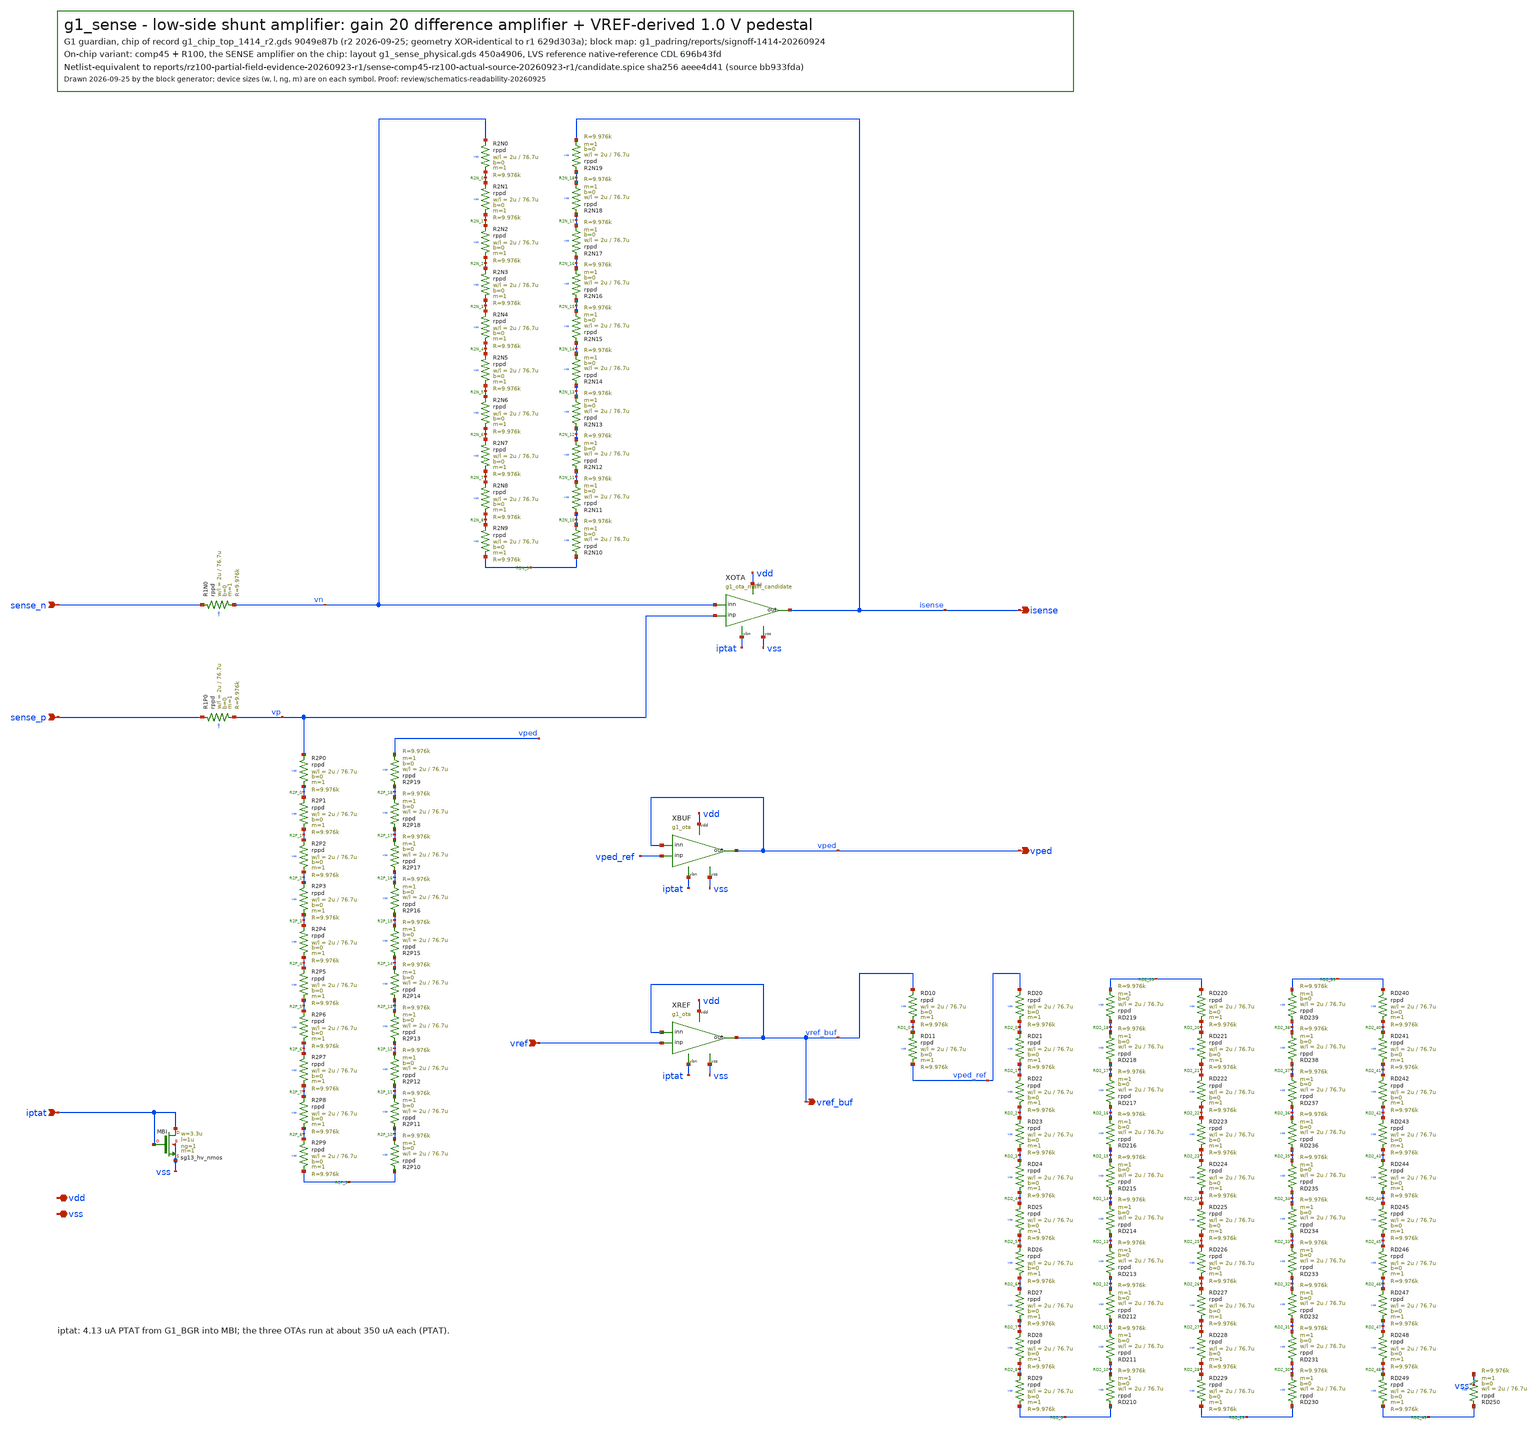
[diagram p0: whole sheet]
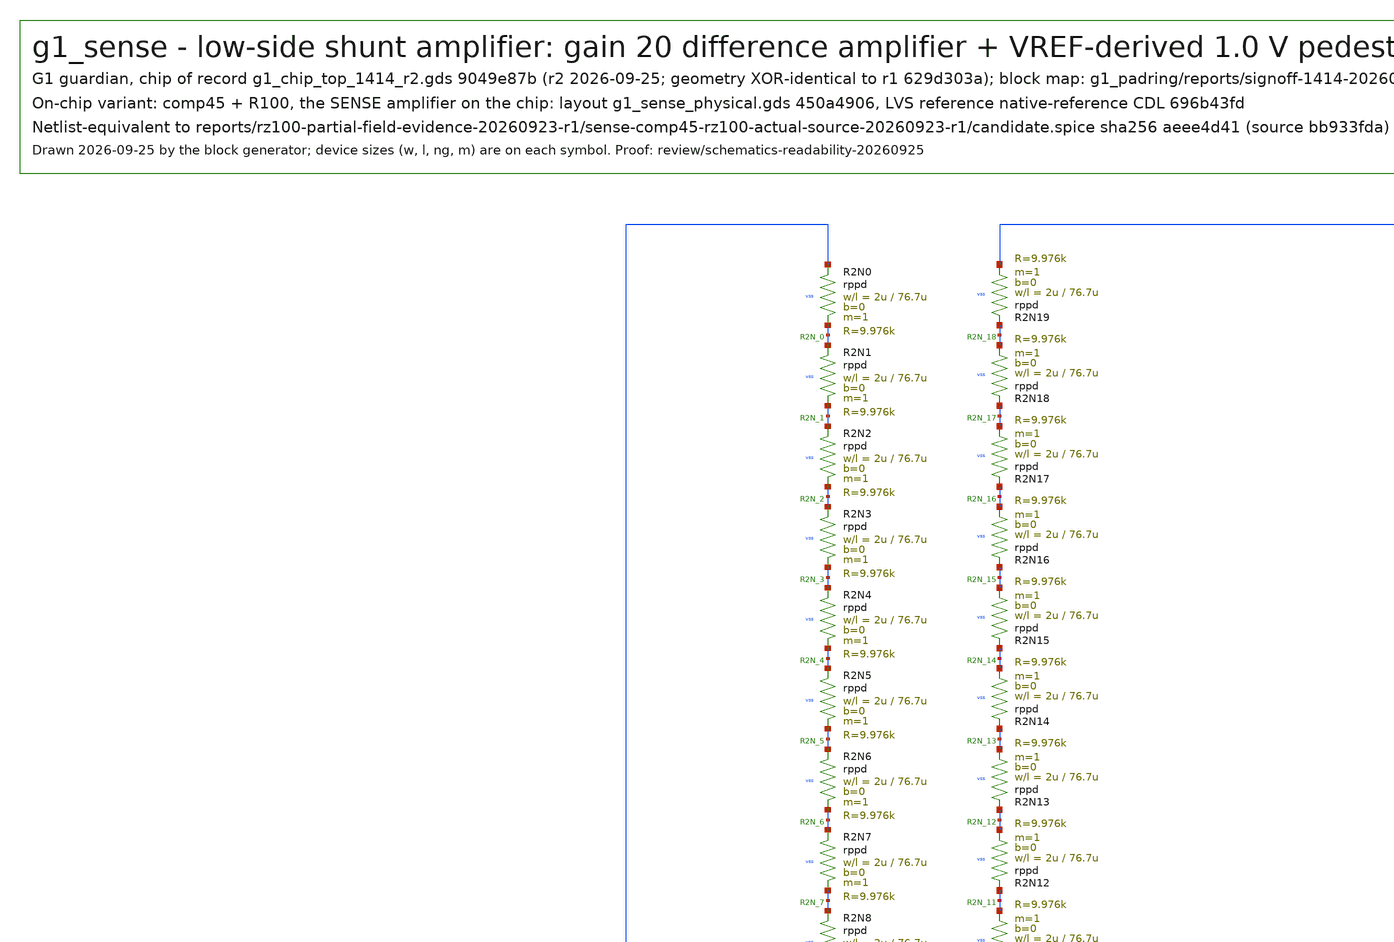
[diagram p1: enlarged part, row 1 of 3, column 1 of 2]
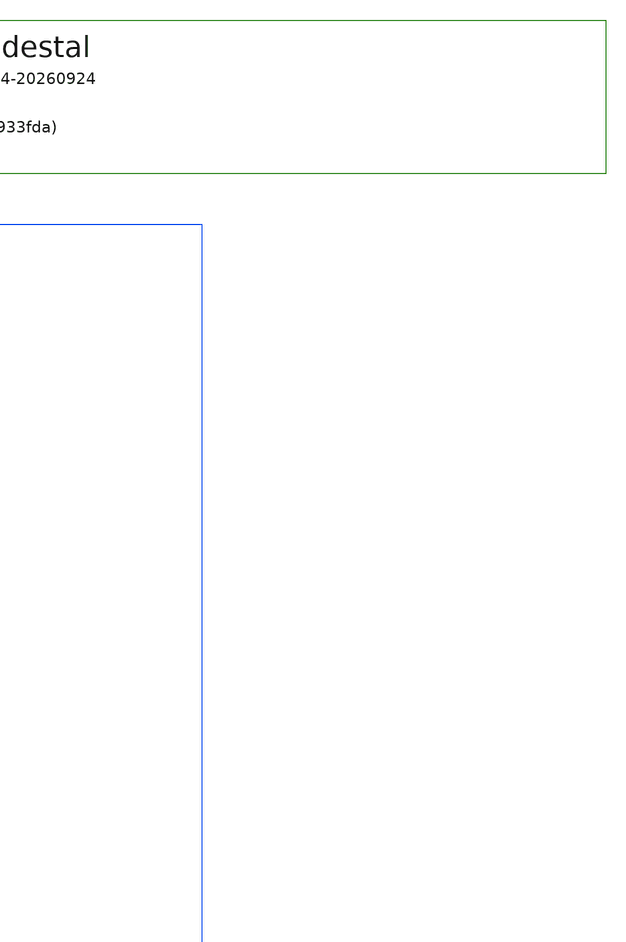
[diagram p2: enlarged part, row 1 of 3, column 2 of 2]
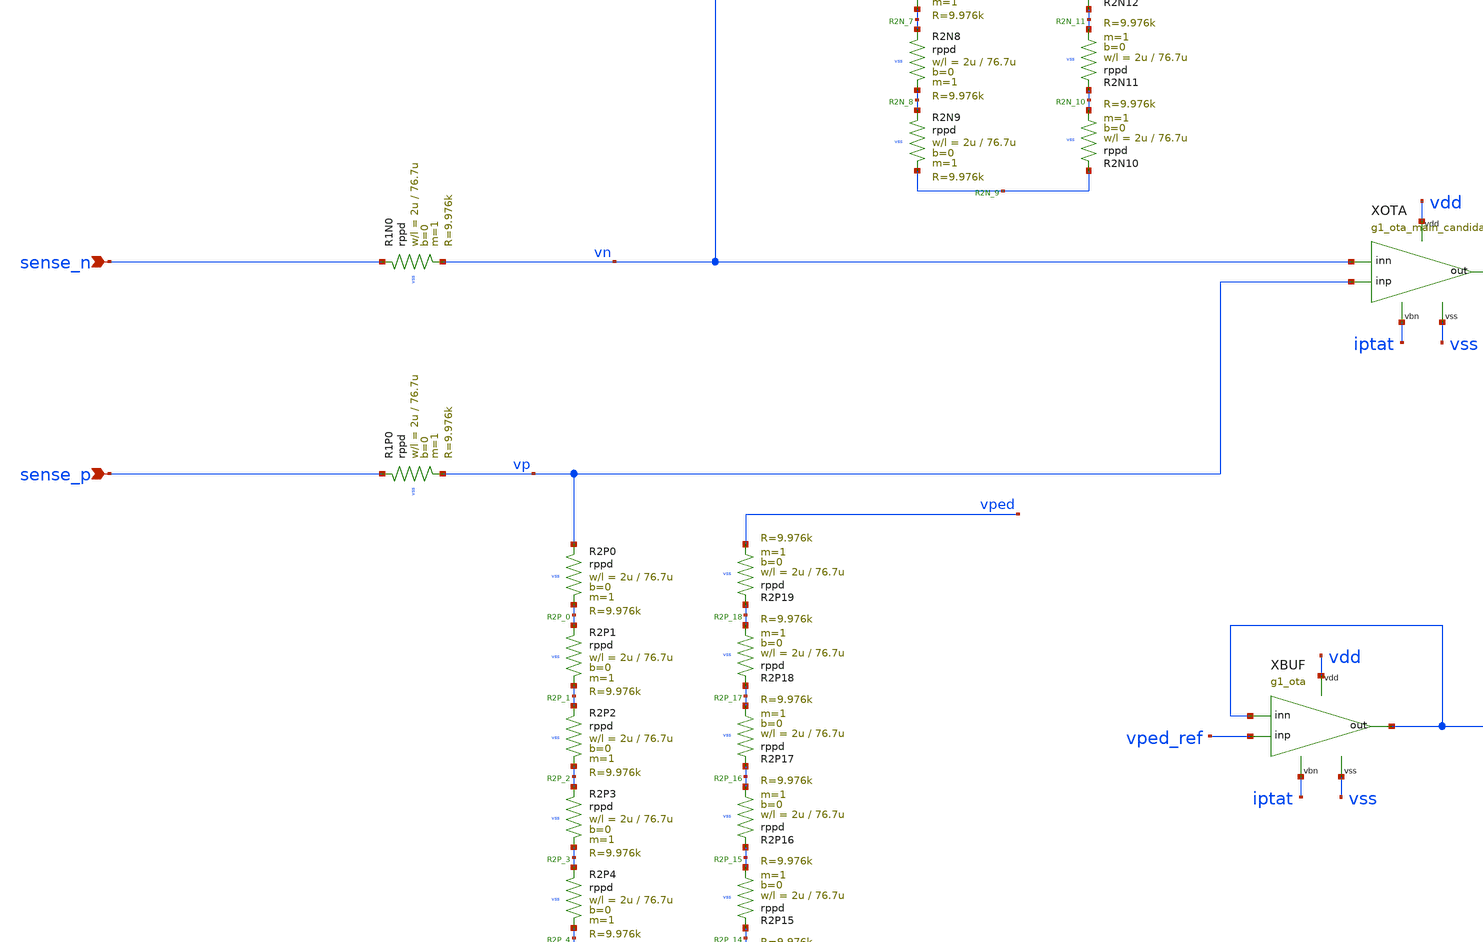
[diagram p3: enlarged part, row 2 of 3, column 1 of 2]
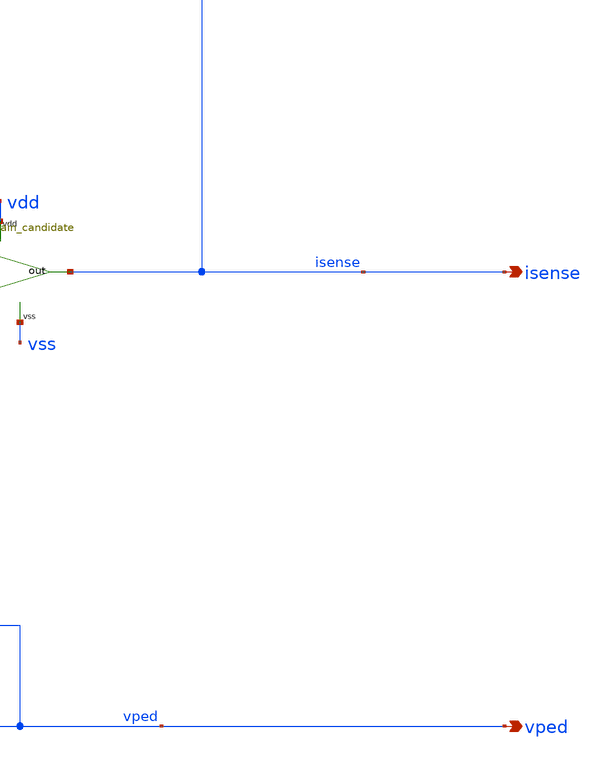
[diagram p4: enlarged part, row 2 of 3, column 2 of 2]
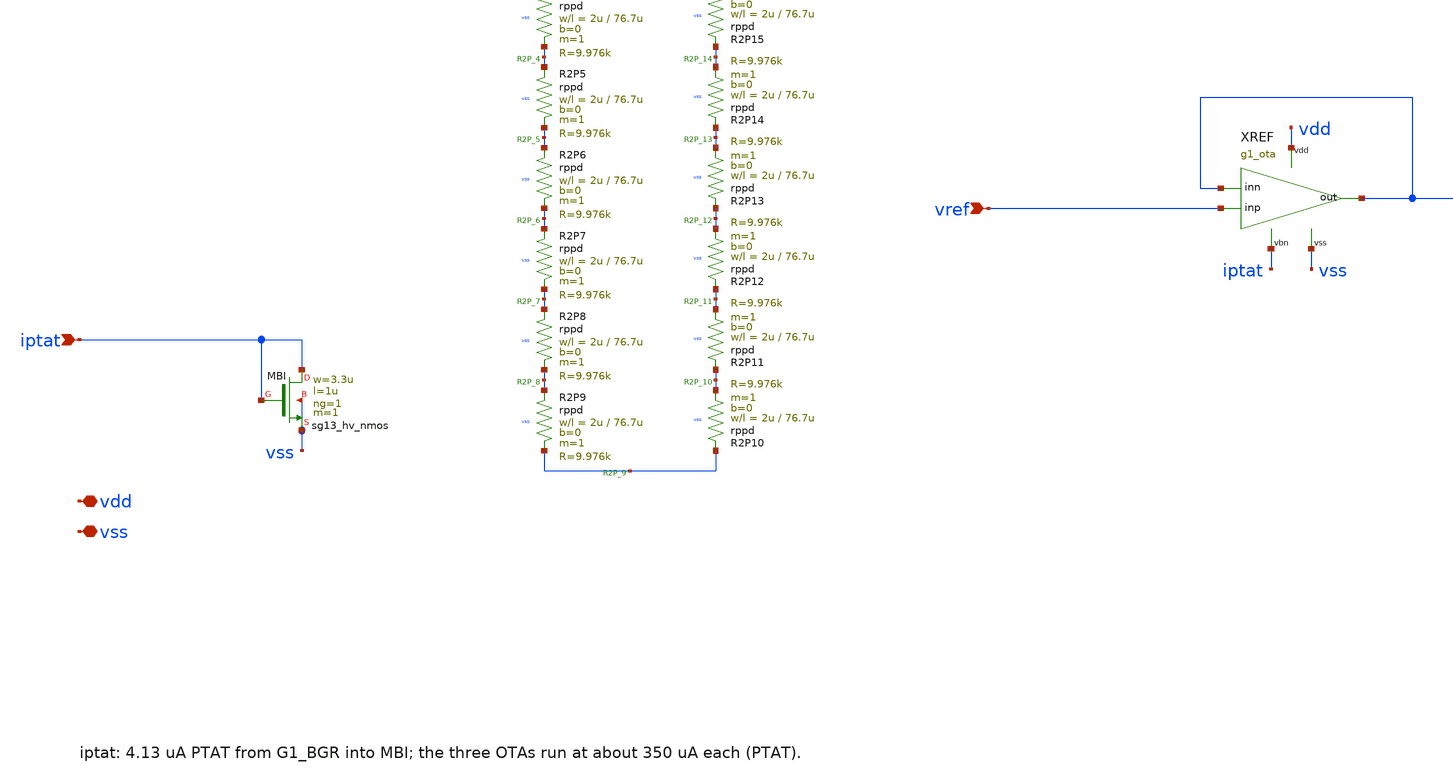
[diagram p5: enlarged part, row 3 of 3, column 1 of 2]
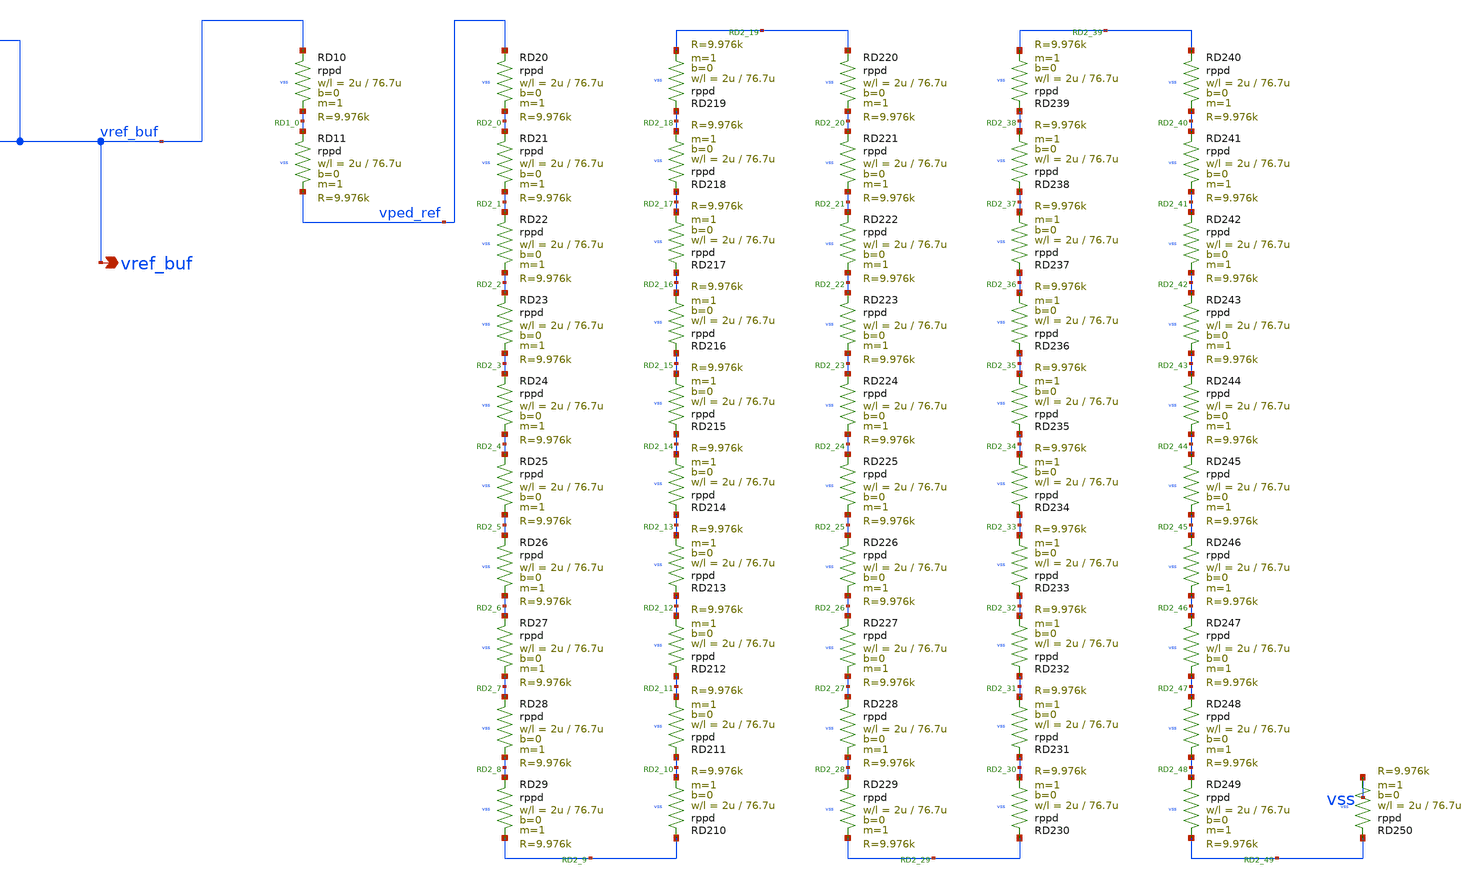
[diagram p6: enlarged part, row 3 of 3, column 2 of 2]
** sch_path: designs/g1-guardian/blocks/g1_sense/xschem/comp45_r100/g1_sense.sch
**.subckt g1_sense sense_p sense_n vref iptat isense vped vref_buf vdd vss
*.ipin sense_p
*.ipin sense_n
*.ipin vref
*.ipin iptat
*.opin isense
*.opin vped
*.opin vref_buf
*.iopin vdd
*.iopin vss
XR1N0 sense_n vn vss rppd w=2u l=76.7u m=1 b=0 mm_ok=1
XR2N0 vn R2N_0 vss rppd w=2u l=76.7u m=1 b=0 mm_ok=1
XR2N1 R2N_0 R2N_1 vss rppd w=2u l=76.7u m=1 b=0 mm_ok=1
XR2N2 R2N_1 R2N_2 vss rppd w=2u l=76.7u m=1 b=0 mm_ok=1
XR2N3 R2N_2 R2N_3 vss rppd w=2u l=76.7u m=1 b=0 mm_ok=1
XR2N4 R2N_3 R2N_4 vss rppd w=2u l=76.7u m=1 b=0 mm_ok=1
XR2N5 R2N_4 R2N_5 vss rppd w=2u l=76.7u m=1 b=0 mm_ok=1
XR2N6 R2N_5 R2N_6 vss rppd w=2u l=76.7u m=1 b=0 mm_ok=1
XR2N7 R2N_6 R2N_7 vss rppd w=2u l=76.7u m=1 b=0 mm_ok=1
XR2N8 R2N_7 R2N_8 vss rppd w=2u l=76.7u m=1 b=0 mm_ok=1
XR2N9 R2N_8 R2N_9 vss rppd w=2u l=76.7u m=1 b=0 mm_ok=1
XR2N10 R2N_9 R2N_10 vss rppd w=2u l=76.7u m=1 b=0 mm_ok=1
XR2N11 R2N_10 R2N_11 vss rppd w=2u l=76.7u m=1 b=0 mm_ok=1
XR2N12 R2N_11 R2N_12 vss rppd w=2u l=76.7u m=1 b=0 mm_ok=1
XR2N13 R2N_12 R2N_13 vss rppd w=2u l=76.7u m=1 b=0 mm_ok=1
XR2N14 R2N_13 R2N_14 vss rppd w=2u l=76.7u m=1 b=0 mm_ok=1
XR2N15 R2N_14 R2N_15 vss rppd w=2u l=76.7u m=1 b=0 mm_ok=1
XR2N16 R2N_15 R2N_16 vss rppd w=2u l=76.7u m=1 b=0 mm_ok=1
XR2N17 R2N_16 R2N_17 vss rppd w=2u l=76.7u m=1 b=0 mm_ok=1
XR2N18 R2N_17 R2N_18 vss rppd w=2u l=76.7u m=1 b=0 mm_ok=1
XR2N19 R2N_18 isense vss rppd w=2u l=76.7u m=1 b=0 mm_ok=1
XR1P0 sense_p vp vss rppd w=2u l=76.7u m=1 b=0 mm_ok=1
XR2P0 vp R2P_0 vss rppd w=2u l=76.7u m=1 b=0 mm_ok=1
XR2P1 R2P_0 R2P_1 vss rppd w=2u l=76.7u m=1 b=0 mm_ok=1
XR2P2 R2P_1 R2P_2 vss rppd w=2u l=76.7u m=1 b=0 mm_ok=1
XR2P3 R2P_2 R2P_3 vss rppd w=2u l=76.7u m=1 b=0 mm_ok=1
XR2P4 R2P_3 R2P_4 vss rppd w=2u l=76.7u m=1 b=0 mm_ok=1
XR2P5 R2P_4 R2P_5 vss rppd w=2u l=76.7u m=1 b=0 mm_ok=1
XR2P6 R2P_5 R2P_6 vss rppd w=2u l=76.7u m=1 b=0 mm_ok=1
XR2P7 R2P_6 R2P_7 vss rppd w=2u l=76.7u m=1 b=0 mm_ok=1
XR2P8 R2P_7 R2P_8 vss rppd w=2u l=76.7u m=1 b=0 mm_ok=1
XR2P9 R2P_8 R2P_9 vss rppd w=2u l=76.7u m=1 b=0 mm_ok=1
XR2P10 R2P_9 R2P_10 vss rppd w=2u l=76.7u m=1 b=0 mm_ok=1
XR2P11 R2P_10 R2P_11 vss rppd w=2u l=76.7u m=1 b=0 mm_ok=1
XR2P12 R2P_11 R2P_12 vss rppd w=2u l=76.7u m=1 b=0 mm_ok=1
XR2P13 R2P_12 R2P_13 vss rppd w=2u l=76.7u m=1 b=0 mm_ok=1
XR2P14 R2P_13 R2P_14 vss rppd w=2u l=76.7u m=1 b=0 mm_ok=1
XR2P15 R2P_14 R2P_15 vss rppd w=2u l=76.7u m=1 b=0 mm_ok=1
XR2P16 R2P_15 R2P_16 vss rppd w=2u l=76.7u m=1 b=0 mm_ok=1
XR2P17 R2P_16 R2P_17 vss rppd w=2u l=76.7u m=1 b=0 mm_ok=1
XR2P18 R2P_17 R2P_18 vss rppd w=2u l=76.7u m=1 b=0 mm_ok=1
XR2P19 R2P_18 vped vss rppd w=2u l=76.7u m=1 b=0 mm_ok=1
XRD10 vref_buf RD1_0 vss rppd w=2u l=76.7u m=1 b=0 mm_ok=1
XRD11 RD1_0 vped_ref vss rppd w=2u l=76.7u m=1 b=0 mm_ok=1
XRD20 vped_ref RD2_0 vss rppd w=2u l=76.7u m=1 b=0 mm_ok=1
XRD21 RD2_0 RD2_1 vss rppd w=2u l=76.7u m=1 b=0 mm_ok=1
XRD22 RD2_1 RD2_2 vss rppd w=2u l=76.7u m=1 b=0 mm_ok=1
XRD23 RD2_2 RD2_3 vss rppd w=2u l=76.7u m=1 b=0 mm_ok=1
XRD24 RD2_3 RD2_4 vss rppd w=2u l=76.7u m=1 b=0 mm_ok=1
XRD25 RD2_4 RD2_5 vss rppd w=2u l=76.7u m=1 b=0 mm_ok=1
XRD26 RD2_5 RD2_6 vss rppd w=2u l=76.7u m=1 b=0 mm_ok=1
XRD27 RD2_6 RD2_7 vss rppd w=2u l=76.7u m=1 b=0 mm_ok=1
XRD28 RD2_7 RD2_8 vss rppd w=2u l=76.7u m=1 b=0 mm_ok=1
XRD29 RD2_8 RD2_9 vss rppd w=2u l=76.7u m=1 b=0 mm_ok=1
XRD210 RD2_9 RD2_10 vss rppd w=2u l=76.7u m=1 b=0 mm_ok=1
XRD211 RD2_10 RD2_11 vss rppd w=2u l=76.7u m=1 b=0 mm_ok=1
XRD212 RD2_11 RD2_12 vss rppd w=2u l=76.7u m=1 b=0 mm_ok=1
XRD213 RD2_12 RD2_13 vss rppd w=2u l=76.7u m=1 b=0 mm_ok=1
XRD214 RD2_13 RD2_14 vss rppd w=2u l=76.7u m=1 b=0 mm_ok=1
XRD215 RD2_14 RD2_15 vss rppd w=2u l=76.7u m=1 b=0 mm_ok=1
XRD216 RD2_15 RD2_16 vss rppd w=2u l=76.7u m=1 b=0 mm_ok=1
XRD217 RD2_16 RD2_17 vss rppd w=2u l=76.7u m=1 b=0 mm_ok=1
XRD218 RD2_17 RD2_18 vss rppd w=2u l=76.7u m=1 b=0 mm_ok=1
XRD219 RD2_18 RD2_19 vss rppd w=2u l=76.7u m=1 b=0 mm_ok=1
XRD220 RD2_19 RD2_20 vss rppd w=2u l=76.7u m=1 b=0 mm_ok=1
XRD221 RD2_20 RD2_21 vss rppd w=2u l=76.7u m=1 b=0 mm_ok=1
XRD222 RD2_21 RD2_22 vss rppd w=2u l=76.7u m=1 b=0 mm_ok=1
XRD223 RD2_22 RD2_23 vss rppd w=2u l=76.7u m=1 b=0 mm_ok=1
XRD224 RD2_23 RD2_24 vss rppd w=2u l=76.7u m=1 b=0 mm_ok=1
XRD225 RD2_24 RD2_25 vss rppd w=2u l=76.7u m=1 b=0 mm_ok=1
XRD226 RD2_25 RD2_26 vss rppd w=2u l=76.7u m=1 b=0 mm_ok=1
XRD227 RD2_26 RD2_27 vss rppd w=2u l=76.7u m=1 b=0 mm_ok=1
XRD228 RD2_27 RD2_28 vss rppd w=2u l=76.7u m=1 b=0 mm_ok=1
XRD229 RD2_28 RD2_29 vss rppd w=2u l=76.7u m=1 b=0 mm_ok=1
XRD230 RD2_29 RD2_30 vss rppd w=2u l=76.7u m=1 b=0 mm_ok=1
XRD231 RD2_30 RD2_31 vss rppd w=2u l=76.7u m=1 b=0 mm_ok=1
XRD232 RD2_31 RD2_32 vss rppd w=2u l=76.7u m=1 b=0 mm_ok=1
XRD233 RD2_32 RD2_33 vss rppd w=2u l=76.7u m=1 b=0 mm_ok=1
XRD234 RD2_33 RD2_34 vss rppd w=2u l=76.7u m=1 b=0 mm_ok=1
XRD235 RD2_34 RD2_35 vss rppd w=2u l=76.7u m=1 b=0 mm_ok=1
XRD236 RD2_35 RD2_36 vss rppd w=2u l=76.7u m=1 b=0 mm_ok=1
XRD237 RD2_36 RD2_37 vss rppd w=2u l=76.7u m=1 b=0 mm_ok=1
XRD238 RD2_37 RD2_38 vss rppd w=2u l=76.7u m=1 b=0 mm_ok=1
XRD239 RD2_38 RD2_39 vss rppd w=2u l=76.7u m=1 b=0 mm_ok=1
XRD240 RD2_39 RD2_40 vss rppd w=2u l=76.7u m=1 b=0 mm_ok=1
XRD241 RD2_40 RD2_41 vss rppd w=2u l=76.7u m=1 b=0 mm_ok=1
XRD242 RD2_41 RD2_42 vss rppd w=2u l=76.7u m=1 b=0 mm_ok=1
XRD243 RD2_42 RD2_43 vss rppd w=2u l=76.7u m=1 b=0 mm_ok=1
XRD244 RD2_43 RD2_44 vss rppd w=2u l=76.7u m=1 b=0 mm_ok=1
XRD245 RD2_44 RD2_45 vss rppd w=2u l=76.7u m=1 b=0 mm_ok=1
XRD246 RD2_45 RD2_46 vss rppd w=2u l=76.7u m=1 b=0 mm_ok=1
XRD247 RD2_46 RD2_47 vss rppd w=2u l=76.7u m=1 b=0 mm_ok=1
XRD248 RD2_47 RD2_48 vss rppd w=2u l=76.7u m=1 b=0 mm_ok=1
XRD249 RD2_48 RD2_49 vss rppd w=2u l=76.7u m=1 b=0 mm_ok=1
XRD250 RD2_49 vss vss rppd w=2u l=76.7u m=1 b=0 mm_ok=1
XMBI iptat iptat vss vss sg13_hv_nmos w=3.3u l=1u ng=1 m=1 mm_ok=1
XOTA vp vn iptat isense vdd vss g1_ota_main_candidate
XBUF vped_ref vped iptat vped vdd vss g1_ota
XREF vref vref_buf iptat vref_buf vdd vss g1_ota
**.ends

* expanding   symbol:  g1_ota_main_candidate.sym # of pins=6
** sym_path: designs/g1-guardian/blocks/g1_sense/xschem/comp45_r100/g1_ota_main_candidate.sym
** sch_path: designs/g1-guardian/blocks/g1_sense/xschem/comp45_r100/g1_ota_main_candidate.sch
.subckt g1_ota_main_candidate inp inn vbn out vdd vss
*.ipin inp
*.ipin inn
*.ipin vbn
*.opin out
*.iopin vdd
*.iopin vss
XMB2 vbp vbn vss vss sg13_hv_nmos w=8u l=1u ng=2 m=1 mm_ok=1
XMB3 vbp vbp vdd vdd sg13_hv_pmos w=16u l=1u ng=4 m=1 mm_ok=1
XMB5 vbnc vbp vdd vdd sg13_hv_pmos w=16u l=1u ng=4 m=1 mm_ok=1
XMB4 vbnc vbnc vss vss sg13_hv_nmos w=1.6u l=1u ng=1 m=1 mm_ok=1
XMB6 vbpc vbn vss vss sg13_hv_nmos w=8u l=1u ng=2 m=1 mm_ok=1
XMB7 vbpc vbpc vdd vdd sg13_hv_pmos w=3.2u l=1u ng=1 m=1 mm_ok=1
XMT tail vbp vdd vdd sg13_hv_pmos w=128u l=1u ng=16 m=1 mm_ok=1
XM1 fn inn tail vdd sg13_hv_pmos w=384u l=2u ng=64 m=1 mm_ok=1
XM2 fp inp tail vdd sg13_hv_pmos w=384u l=2u ng=64 m=1 mm_ok=1
XM3 fn vbn vss vss sg13_hv_nmos w=320u l=4u ng=40 m=1 mm_ok=1
XM4 fp vbn vss vss sg13_hv_nmos w=320u l=4u ng=40 m=1 mm_ok=1
XM13 mir vbnc fn vss sg13_hv_nmos w=48u l=1u ng=6 m=1 mm_ok=1
XM16 out1 vbnc fp vss sg13_hv_nmos w=48u l=1u ng=6 m=1 mm_ok=1
XM14 pc1 mir vdd vdd sg13_hv_pmos w=384u l=4u ng=48 m=1 mm_ok=1
XM11 pc2 mir vdd vdd sg13_hv_pmos w=384u l=4u ng=48 m=1 mm_ok=1
XM15 mir vbpc pc1 vdd sg13_hv_pmos w=384u l=4u ng=48 m=1 mm_ok=1
XM12 out1 vbpc pc2 vdd sg13_hv_pmos w=384u l=4u ng=48 m=1 mm_ok=1
XM20 out out1 vdd vdd sg13_hv_pmos w=192u l=1u ng=24 m=1 mm_ok=1
XM21 out vbn vss vss sg13_hv_nmos w=96u l=1u ng=12 m=1 mm_ok=1
XRZ out1 cz vss rppd w=1u l=100u m=1 b=0 mm_ok=1
XCC cz out cap_cmim w=45u l=23u m=1 mm_ok=1
.ends


* expanding   symbol:  g1_ota.sym # of pins=6
** sym_path: designs/g1-guardian/blocks/g1_sense/xschem/comp45_r100/g1_ota.sym
** sch_path: designs/g1-guardian/blocks/g1_sense/xschem/comp45_r100/g1_ota.sch
.subckt g1_ota inp inn vbn out vdd vss
*.ipin inp
*.ipin inn
*.ipin vbn
*.opin out
*.iopin vdd
*.iopin vss
XMB2 vbp vbn vss vss sg13_hv_nmos w=8u l=1u ng=2 m=1 mm_ok=1
XMB3 vbp vbp vdd vdd sg13_hv_pmos w=16u l=1u ng=4 m=1 mm_ok=1
XMB5 vbnc vbp vdd vdd sg13_hv_pmos w=16u l=1u ng=4 m=1 mm_ok=1
XMB4 vbnc vbnc vss vss sg13_hv_nmos w=1.6u l=1u ng=1 m=1 mm_ok=1
XMB6 vbpc vbn vss vss sg13_hv_nmos w=8u l=1u ng=2 m=1 mm_ok=1
XMB7 vbpc vbpc vdd vdd sg13_hv_pmos w=3.2u l=1u ng=1 m=1 mm_ok=1
XMT tail vbp vdd vdd sg13_hv_pmos w=128u l=1u ng=16 m=1 mm_ok=1
XM1 fn inn tail vdd sg13_hv_pmos w=96u l=2u ng=16 m=1 mm_ok=1
XM2 fp inp tail vdd sg13_hv_pmos w=96u l=2u ng=16 m=1 mm_ok=1
XM3 fn vbn vss vss sg13_hv_nmos w=80u l=1u ng=10 m=1 mm_ok=1
XM4 fp vbn vss vss sg13_hv_nmos w=80u l=1u ng=10 m=1 mm_ok=1
XM13 mir vbnc fn vss sg13_hv_nmos w=48u l=1u ng=6 m=1 mm_ok=1
XM16 out1 vbnc fp vss sg13_hv_nmos w=48u l=1u ng=6 m=1 mm_ok=1
XM14 pc1 mir vdd vdd sg13_hv_pmos w=96u l=1u ng=12 m=1 mm_ok=1
XM11 pc2 mir vdd vdd sg13_hv_pmos w=96u l=1u ng=12 m=1 mm_ok=1
XM15 mir vbpc pc1 vdd sg13_hv_pmos w=96u l=1u ng=12 m=1 mm_ok=1
XM12 out1 vbpc pc2 vdd sg13_hv_pmos w=96u l=1u ng=12 m=1 mm_ok=1
XM20 out out1 vdd vdd sg13_hv_pmos w=192u l=1u ng=24 m=1 mm_ok=1
XM21 out vbn vss vss sg13_hv_nmos w=96u l=1u ng=12 m=1 mm_ok=1
XRZ out1 cz vss rppd w=1u l=6.2u m=1 b=0 mm_ok=1
XCC cz out cap_cmim w=23u l=23u m=1 mm_ok=1
.ends

.end
